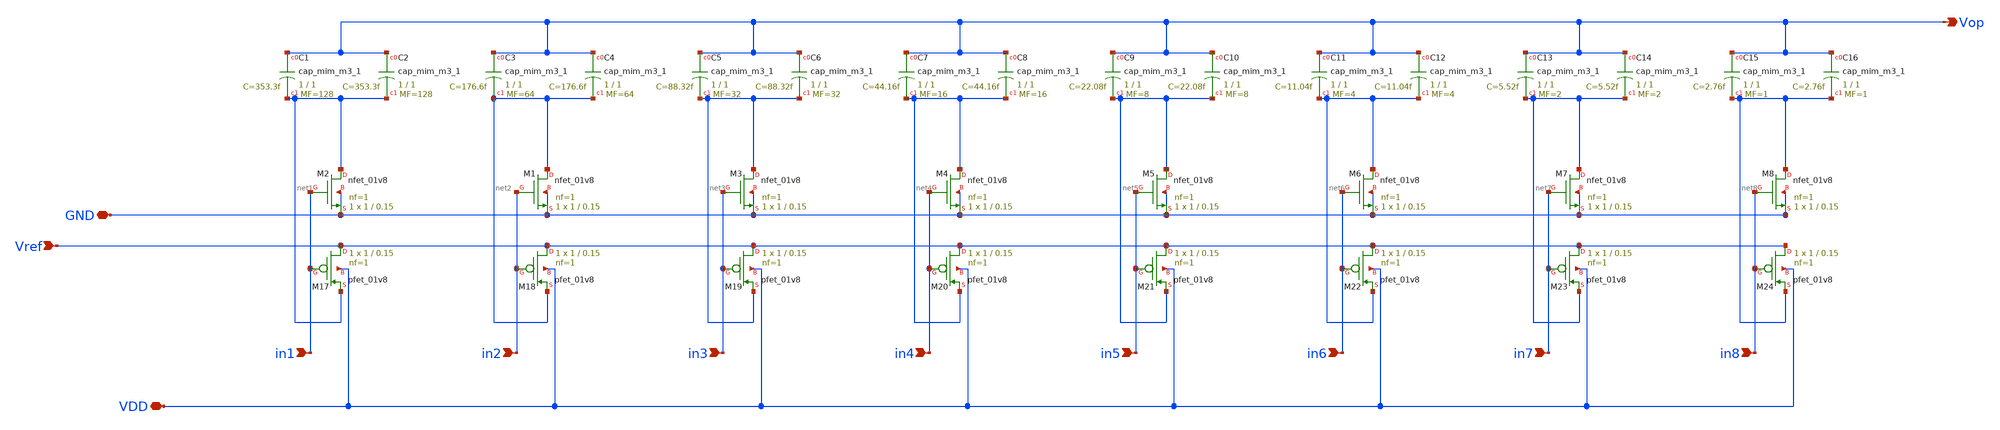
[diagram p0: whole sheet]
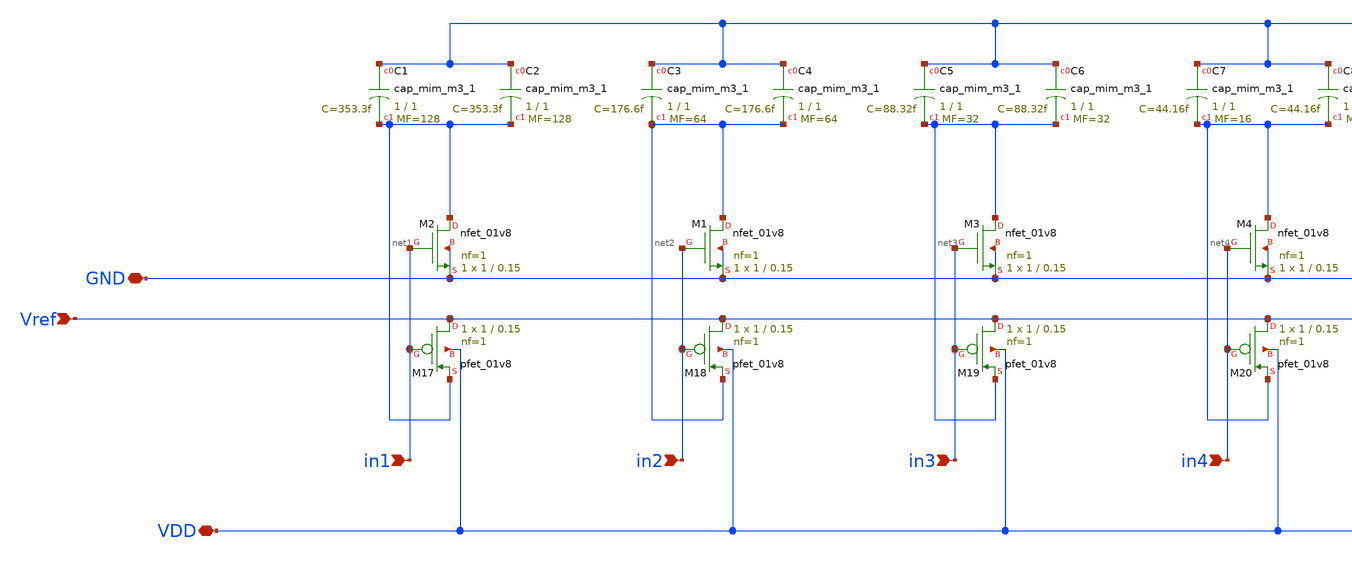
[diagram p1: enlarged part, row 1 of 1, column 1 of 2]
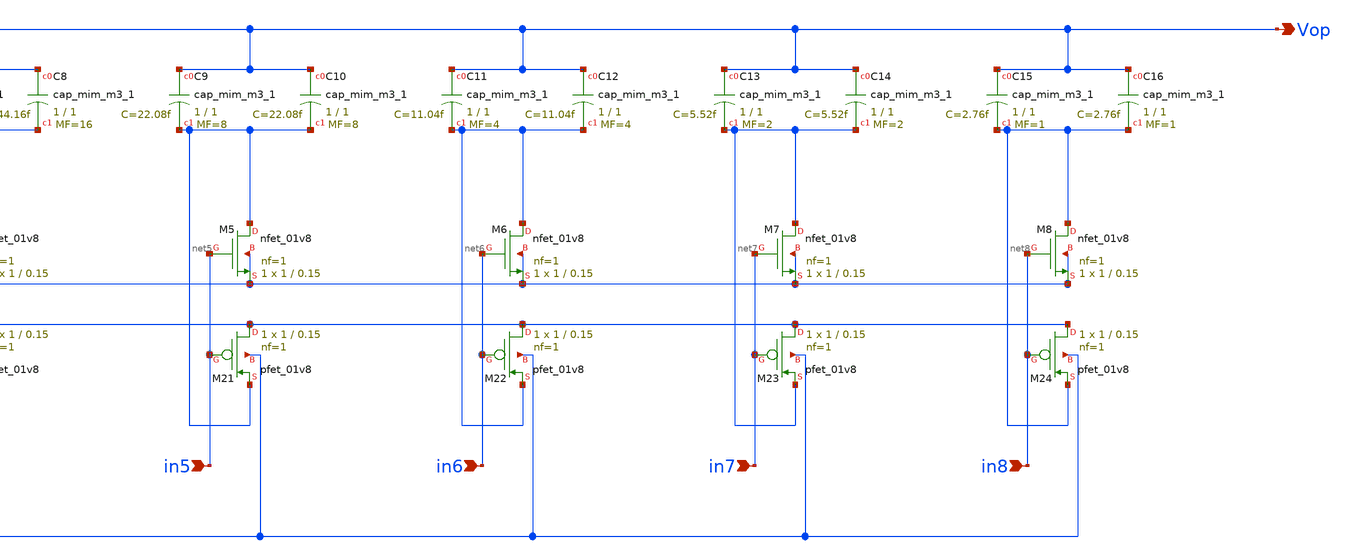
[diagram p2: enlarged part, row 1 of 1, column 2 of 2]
** sch_path: sar-adc/updated/sin-cdac_wotg.sch
**.subckt sin-cdac_wotg Vref VDD Vop GND in1 in2 in3 in4 in5 in6 in7 in8
*.ipin Vref
*.iopin VDD
*.opin Vop
*.iopin GND
*.ipin in1
*.ipin in2
*.ipin in3
*.ipin in4
*.ipin in5
*.ipin in6
*.ipin in7
*.ipin in8
XC1 Vop net1 sky130_fd_pr__cap_mim_m3_1 W=1 L=1 MF=128 m=128
XC3 Vop net2 sky130_fd_pr__cap_mim_m3_1 W=1 L=1 MF=64 m=64
XC4 Vop net2 sky130_fd_pr__cap_mim_m3_1 W=1 L=1 MF=64 m=64
XC5 Vop net3 sky130_fd_pr__cap_mim_m3_1 W=1 L=1 MF=32 m=32
XC6 Vop net3 sky130_fd_pr__cap_mim_m3_1 W=1 L=1 MF=32 m=32
XC7 Vop net4 sky130_fd_pr__cap_mim_m3_1 W=1 L=1 MF=16 m=16
XC8 Vop net4 sky130_fd_pr__cap_mim_m3_1 W=1 L=1 MF=16 m=16
XC9 Vop net5 sky130_fd_pr__cap_mim_m3_1 W=1 L=1 MF=8 m=8
XC10 Vop net5 sky130_fd_pr__cap_mim_m3_1 W=1 L=1 MF=8 m=8
XC11 Vop net6 sky130_fd_pr__cap_mim_m3_1 W=1 L=1 MF=4 m=4
XC12 Vop net6 sky130_fd_pr__cap_mim_m3_1 W=1 L=1 MF=4 m=4
XC13 Vop net7 sky130_fd_pr__cap_mim_m3_1 W=1 L=1 MF=2 m=2
XC14 Vop net7 sky130_fd_pr__cap_mim_m3_1 W=1 L=1 MF=2 m=2
XC15 Vop net8 sky130_fd_pr__cap_mim_m3_1 W=1 L=1 MF=1 m=1
XC16 Vop net8 sky130_fd_pr__cap_mim_m3_1 W=1 L=1 MF=1 m=1
XM2 net1 in1 GND GND sky130_fd_pr__nfet_01v8 L=0.15 W=1 nf=1 ad='int((1 + 1)/2) * 1 / 1 * 0.29' as='int((1 + 2)/2) * 1 / 1 * 0.29'
+ pd='2*int((1 + 1)/2) * (1 / 1 + 0.29)' ps='2*int((1 + 2)/2) * (1 / 1 + 0.29)' nrd='0.29 / 1 ' nrs='0.29 / 1 '
+ sa=0 sb=0 sd=0 mult=1 m=1
XM1 net2 in2 GND GND sky130_fd_pr__nfet_01v8 L=0.15 W=1 nf=1 ad='int((1 + 1)/2) * 1 / 1 * 0.29' as='int((1 + 2)/2) * 1 / 1 * 0.29'
+ pd='2*int((1 + 1)/2) * (1 / 1 + 0.29)' ps='2*int((1 + 2)/2) * (1 / 1 + 0.29)' nrd='0.29 / 1 ' nrs='0.29 / 1 '
+ sa=0 sb=0 sd=0 mult=1 m=1
XM3 net3 in3 GND GND sky130_fd_pr__nfet_01v8 L=0.15 W=1 nf=1 ad='int((1 + 1)/2) * 1 / 1 * 0.29' as='int((1 + 2)/2) * 1 / 1 * 0.29'
+ pd='2*int((1 + 1)/2) * (1 / 1 + 0.29)' ps='2*int((1 + 2)/2) * (1 / 1 + 0.29)' nrd='0.29 / 1 ' nrs='0.29 / 1 '
+ sa=0 sb=0 sd=0 mult=1 m=1
XM4 net4 in4 GND GND sky130_fd_pr__nfet_01v8 L=0.15 W=1 nf=1 ad='int((1 + 1)/2) * 1 / 1 * 0.29' as='int((1 + 2)/2) * 1 / 1 * 0.29'
+ pd='2*int((1 + 1)/2) * (1 / 1 + 0.29)' ps='2*int((1 + 2)/2) * (1 / 1 + 0.29)' nrd='0.29 / 1 ' nrs='0.29 / 1 '
+ sa=0 sb=0 sd=0 mult=1 m=1
XM5 net5 in5 GND GND sky130_fd_pr__nfet_01v8 L=0.15 W=1 nf=1 ad='int((1 + 1)/2) * 1 / 1 * 0.29' as='int((1 + 2)/2) * 1 / 1 * 0.29'
+ pd='2*int((1 + 1)/2) * (1 / 1 + 0.29)' ps='2*int((1 + 2)/2) * (1 / 1 + 0.29)' nrd='0.29 / 1 ' nrs='0.29 / 1 '
+ sa=0 sb=0 sd=0 mult=1 m=1
XM6 net6 in6 GND GND sky130_fd_pr__nfet_01v8 L=0.15 W=1 nf=1 ad='int((1 + 1)/2) * 1 / 1 * 0.29' as='int((1 + 2)/2) * 1 / 1 * 0.29'
+ pd='2*int((1 + 1)/2) * (1 / 1 + 0.29)' ps='2*int((1 + 2)/2) * (1 / 1 + 0.29)' nrd='0.29 / 1 ' nrs='0.29 / 1 '
+ sa=0 sb=0 sd=0 mult=1 m=1
XM7 net7 in7 GND GND sky130_fd_pr__nfet_01v8 L=0.15 W=1 nf=1 ad='int((1 + 1)/2) * 1 / 1 * 0.29' as='int((1 + 2)/2) * 1 / 1 * 0.29'
+ pd='2*int((1 + 1)/2) * (1 / 1 + 0.29)' ps='2*int((1 + 2)/2) * (1 / 1 + 0.29)' nrd='0.29 / 1 ' nrs='0.29 / 1 '
+ sa=0 sb=0 sd=0 mult=1 m=1
XM8 net8 in8 GND GND sky130_fd_pr__nfet_01v8 L=0.15 W=1 nf=1 ad='int((1 + 1)/2) * 1 / 1 * 0.29' as='int((1 + 2)/2) * 1 / 1 * 0.29'
+ pd='2*int((1 + 1)/2) * (1 / 1 + 0.29)' ps='2*int((1 + 2)/2) * (1 / 1 + 0.29)' nrd='0.29 / 1 ' nrs='0.29 / 1 '
+ sa=0 sb=0 sd=0 mult=1 m=1
XM17 Vref in1 net1 VDD sky130_fd_pr__pfet_01v8 L=0.15 W=1 nf=1 ad='int((nf+1)/2) * W/nf * 0.29' as='int((nf+2)/2) * W/nf * 0.29'
+ pd='2*int((nf+1)/2) * (W/nf + 0.29)' ps='2*int((nf+2)/2) * (W/nf + 0.29)' nrd='0.29 / W' nrs='0.29 / W'
+ sa=0 sb=0 sd=0 mult=1 m=1
XM18 Vref in2 net2 VDD sky130_fd_pr__pfet_01v8 L=0.15 W=1 nf=1 ad='int((nf+1)/2) * W/nf * 0.29' as='int((nf+2)/2) * W/nf * 0.29'
+ pd='2*int((nf+1)/2) * (W/nf + 0.29)' ps='2*int((nf+2)/2) * (W/nf + 0.29)' nrd='0.29 / W' nrs='0.29 / W'
+ sa=0 sb=0 sd=0 mult=1 m=1
XM19 Vref in3 net3 VDD sky130_fd_pr__pfet_01v8 L=0.15 W=1 nf=1 ad='int((nf+1)/2) * W/nf * 0.29' as='int((nf+2)/2) * W/nf * 0.29'
+ pd='2*int((nf+1)/2) * (W/nf + 0.29)' ps='2*int((nf+2)/2) * (W/nf + 0.29)' nrd='0.29 / W' nrs='0.29 / W'
+ sa=0 sb=0 sd=0 mult=1 m=1
XM20 Vref in4 net4 VDD sky130_fd_pr__pfet_01v8 L=0.15 W=1 nf=1 ad='int((nf+1)/2) * W/nf * 0.29' as='int((nf+2)/2) * W/nf * 0.29'
+ pd='2*int((nf+1)/2) * (W/nf + 0.29)' ps='2*int((nf+2)/2) * (W/nf + 0.29)' nrd='0.29 / W' nrs='0.29 / W'
+ sa=0 sb=0 sd=0 mult=1 m=1
XM21 Vref in5 net5 VDD sky130_fd_pr__pfet_01v8 L=0.15 W=1 nf=1 ad='int((nf+1)/2) * W/nf * 0.29' as='int((nf+2)/2) * W/nf * 0.29'
+ pd='2*int((nf+1)/2) * (W/nf + 0.29)' ps='2*int((nf+2)/2) * (W/nf + 0.29)' nrd='0.29 / W' nrs='0.29 / W'
+ sa=0 sb=0 sd=0 mult=1 m=1
XM22 Vref in6 net6 VDD sky130_fd_pr__pfet_01v8 L=0.15 W=1 nf=1 ad='int((nf+1)/2) * W/nf * 0.29' as='int((nf+2)/2) * W/nf * 0.29'
+ pd='2*int((nf+1)/2) * (W/nf + 0.29)' ps='2*int((nf+2)/2) * (W/nf + 0.29)' nrd='0.29 / W' nrs='0.29 / W'
+ sa=0 sb=0 sd=0 mult=1 m=1
XM23 Vref in7 net7 VDD sky130_fd_pr__pfet_01v8 L=0.15 W=1 nf=1 ad='int((nf+1)/2) * W/nf * 0.29' as='int((nf+2)/2) * W/nf * 0.29'
+ pd='2*int((nf+1)/2) * (W/nf + 0.29)' ps='2*int((nf+2)/2) * (W/nf + 0.29)' nrd='0.29 / W' nrs='0.29 / W'
+ sa=0 sb=0 sd=0 mult=1 m=1
XM24 Vref in8 net8 VDD sky130_fd_pr__pfet_01v8 L=0.15 W=1 nf=1 ad='int((nf+1)/2) * W/nf * 0.29' as='int((nf+2)/2) * W/nf * 0.29'
+ pd='2*int((nf+1)/2) * (W/nf + 0.29)' ps='2*int((nf+2)/2) * (W/nf + 0.29)' nrd='0.29 / W' nrs='0.29 / W'
+ sa=0 sb=0 sd=0 mult=1 m=1
XC2 Vop net1 sky130_fd_pr__cap_mim_m3_1 W=1 L=1 MF=128 m=128
**.ends
.end
